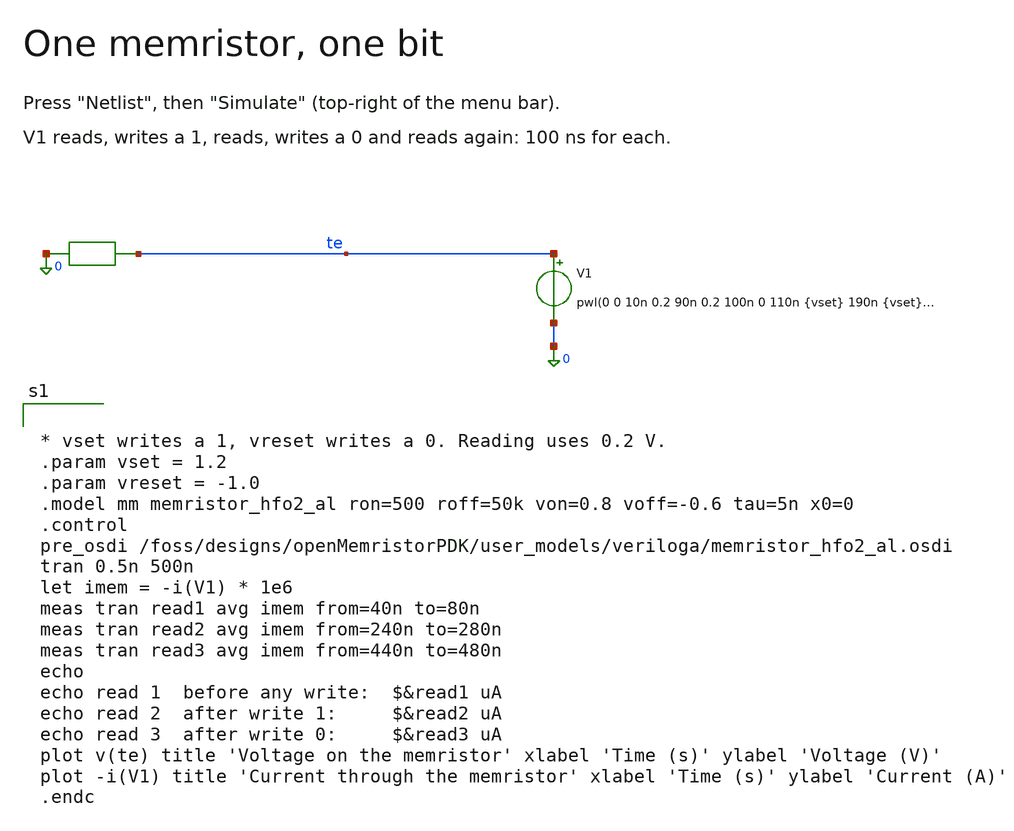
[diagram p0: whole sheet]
** sch_path: libraries/openmemristorpdk_pr/memristor_hfo2_al_bit_tb.sch
**.subckt memristor_hfo2_al_bit_tb
n1 te 0 mm
V1 te 0 pwl(0 0 10n 0.2 90n 0.2 100n 0 110n {vset} 190n {vset} 200n 0 210n 0.2 290n 0.2 300n 0 310n {vreset}
+ 390n {vreset} 400n 0 410n 0.2 490n 0.2 500n 0)
**** begin user architecture code


* vset writes a 1, vreset writes a 0. Reading uses 0.2 V.
.param vset = 1.2
.param vreset = -1.0
.model mm memristor_hfo2_al ron=500 roff=50k von=0.8 voff=-0.6 tau=5n x0=0
.control
pre_osdi /foss/designs/openMemristorPDK/user_models/veriloga/memristor_hfo2_al.osdi
tran 0.5n 500n
let imem = -i(V1) * 1e6
meas tran read1 avg imem from=40n to=80n
meas tran read2 avg imem from=240n to=280n
meas tran read3 avg imem from=440n to=480n
echo
echo read 1  before any write:  $&read1 uA
echo read 2  after write 1:     $&read2 uA
echo read 3  after write 0:     $&read3 uA
plot v(te) title 'Voltage on the memristor' xlabel 'Time (s)' ylabel 'Voltage (V)'
plot -i(V1) title 'Current through the memristor' xlabel 'Time (s)' ylabel 'Current (A)'
.endc


**** end user architecture code
**.ends
.end
